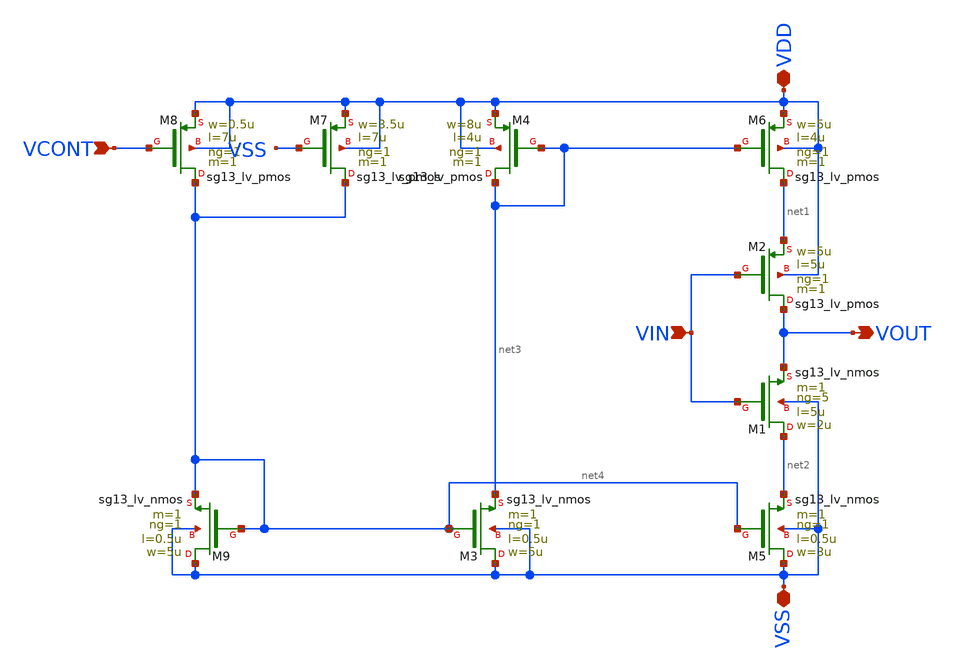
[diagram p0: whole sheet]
** sch_path: xschem/stagehv_v1p1_IHP.sch
**.subckt stagehv_v1p1_IHP VIN VOUT VDD VSS VCONT
*.ipin VIN
*.opin VOUT
*.iopin VDD
*.iopin VSS
*.ipin VCONT
XM9 VSS net4 net4 VSS sg13_lv_nmos w=5u l=0.5u ng=1 m=1 mm_ok=1
XM3 VSS net4 net3 VSS sg13_lv_nmos w=5u l=0.5u ng=1 m=1 mm_ok=1
XM5 VSS net4 net2 VSS sg13_lv_nmos w=3u l=0.5u ng=1 m=1 mm_ok=1
XM8 net4 VCONT VDD VDD sg13_lv_pmos w=0.5u l=7u ng=1 m=1 mm_ok=1
XM4 net3 net3 VDD VDD sg13_lv_pmos w=8u l=4u ng=1 m=1 mm_ok=1
XM6 net1 net3 VDD VDD sg13_lv_pmos w=5u l=4u ng=1 m=1 mm_ok=1
XM2 VOUT VIN net1 VDD sg13_lv_pmos w=5u l=5u ng=1 m=1 mm_ok=1
XM1 net2 VIN VOUT VSS sg13_lv_nmos w=2u l=5u ng=5 m=1 mm_ok=1
XM7 net4 VSS VDD VDD sg13_lv_pmos w=3.5u l=7u ng=1 m=1 mm_ok=1
**.ends
.end
